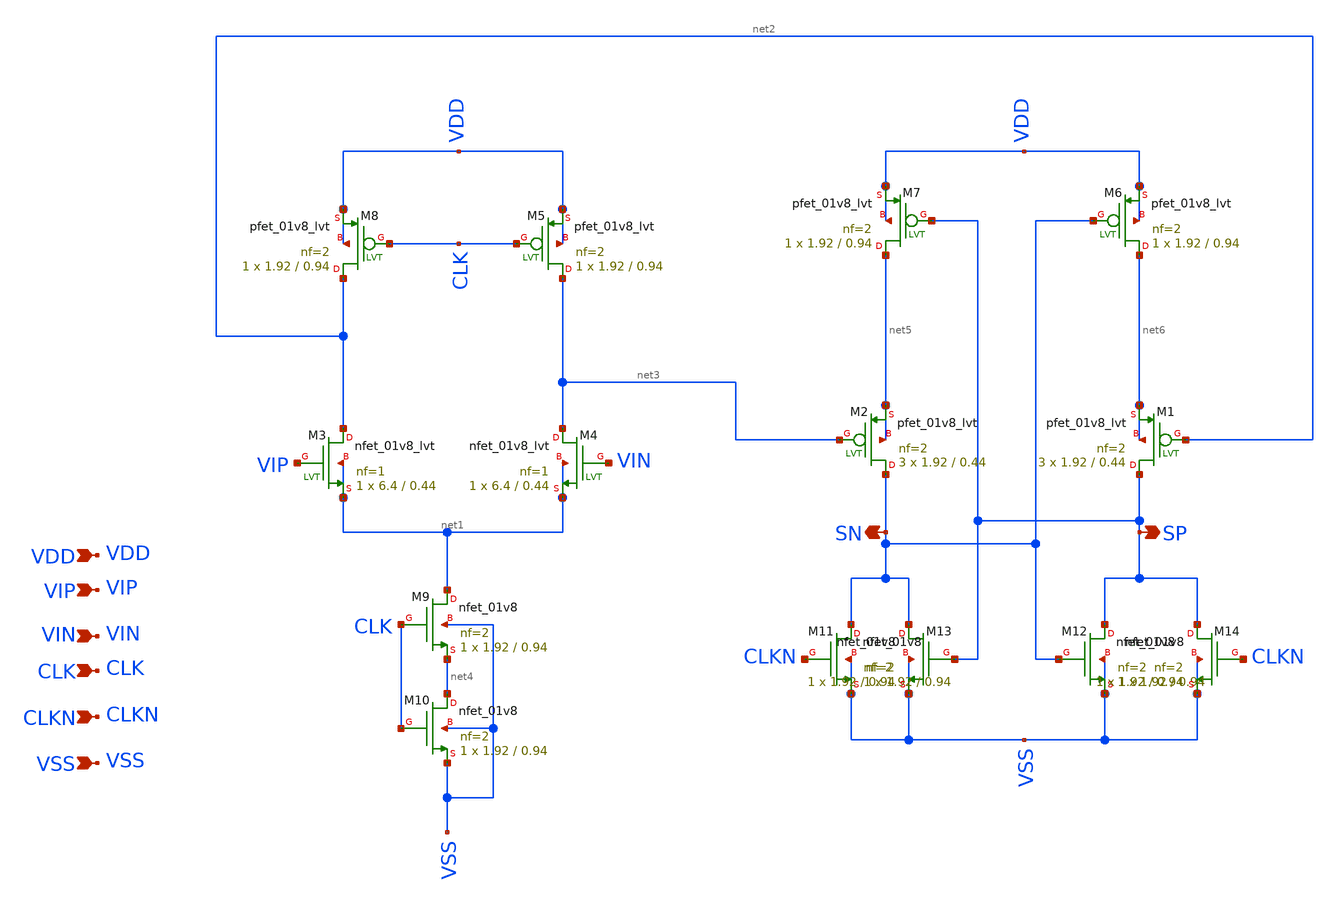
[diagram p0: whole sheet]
** sch_path: design/LELO_SVOD_SKY130A/LELO_CMP.sch
**.subckt LELO_CMP VIP VIN CLK CLKN VDD VSS SN SP
*.ipin VIP
*.ipin VIN
*.ipin CLK
*.ipin CLKN
*.ipin VDD
*.ipin VSS
*.opin SN
*.opin SP
XM2 SN net3 net5 net5 sky130_fd_pr__pfet_01v8_lvt L=0.44 W=1.92 nf=2 ad='int((2 + 1)/2) * 1.92 / 2 * 0.29'
+ as='int((2 + 2)/2) * 1.92 / 2 * 0.29' pd='2*int((2 + 1)/2) * (1.92 / 2 + 0.29)' ps='2*int((2 + 2)/2) * (1.92 / 2 + 0.29)'
+ nrd='0.29 / 1.92 ' nrs='0.29 / 1.92 ' sa=0 sb=0 sd=0 mult=3 m=3
XM1 SP net2 net6 net6 sky130_fd_pr__pfet_01v8_lvt L=0.44 W=1.92 nf=2 ad='int((2 + 1)/2) * 1.92 / 2 * 0.29'
+ as='int((2 + 2)/2) * 1.92 / 2 * 0.29' pd='2*int((2 + 1)/2) * (1.92 / 2 + 0.29)' ps='2*int((2 + 2)/2) * (1.92 / 2 + 0.29)'
+ nrd='0.29 / 1.92 ' nrs='0.29 / 1.92 ' sa=0 sb=0 sd=0 mult=3 m=3
XM3 net2 VIP net1 net1 sky130_fd_pr__nfet_01v8_lvt L=0.44 W=6.4 nf=1 ad='int((1 + 1)/2) * 6.4 / 1 * 0.29'
+ as='int((1 + 2)/2) * 6.4 / 1 * 0.29' pd='2*int((1 + 1)/2) * (6.4 / 1 + 0.29)' ps='2*int((1 + 2)/2) * (6.4 / 1 + 0.29)'
+ nrd='0.29 / 6.4 ' nrs='0.29 / 6.4 ' sa=0 sb=0 sd=0 mult=1 m=1
XM4 net3 VIN net1 net1 sky130_fd_pr__nfet_01v8_lvt L=0.44 W=6.4 nf=1 ad='int((1 + 1)/2) * 6.4 / 1 * 0.29'
+ as='int((1 + 2)/2) * 6.4 / 1 * 0.29' pd='2*int((1 + 1)/2) * (6.4 / 1 + 0.29)' ps='2*int((1 + 2)/2) * (6.4 / 1 + 0.29)'
+ nrd='0.29 / 6.4 ' nrs='0.29 / 6.4 ' sa=0 sb=0 sd=0 mult=1 m=1
XM5 net3 CLK VDD VDD sky130_fd_pr__pfet_01v8_lvt L=0.94 W=1.92 nf=2 ad='int((2 + 1)/2) * 1.92 / 2 * 0.29'
+ as='int((2 + 2)/2) * 1.92 / 2 * 0.29' pd='2*int((2 + 1)/2) * (1.92 / 2 + 0.29)' ps='2*int((2 + 2)/2) * (1.92 / 2 + 0.29)'
+ nrd='0.29 / 1.92 ' nrs='0.29 / 1.92 ' sa=0 sb=0 sd=0 mult=1 m=1
XM6 net6 SN VDD VDD sky130_fd_pr__pfet_01v8_lvt L=0.94 W=1.92 nf=2 ad='int((2 + 1)/2) * 1.92 / 2 * 0.29'
+ as='int((2 + 2)/2) * 1.92 / 2 * 0.29' pd='2*int((2 + 1)/2) * (1.92 / 2 + 0.29)' ps='2*int((2 + 2)/2) * (1.92 / 2 + 0.29)'
+ nrd='0.29 / 1.92 ' nrs='0.29 / 1.92 ' sa=0 sb=0 sd=0 mult=1 m=1
XM7 net5 SP VDD VDD sky130_fd_pr__pfet_01v8_lvt L=0.94 W=1.92 nf=2 ad='int((2 + 1)/2) * 1.92 / 2 * 0.29'
+ as='int((2 + 2)/2) * 1.92 / 2 * 0.29' pd='2*int((2 + 1)/2) * (1.92 / 2 + 0.29)' ps='2*int((2 + 2)/2) * (1.92 / 2 + 0.29)'
+ nrd='0.29 / 1.92 ' nrs='0.29 / 1.92 ' sa=0 sb=0 sd=0 mult=1 m=1
XM8 net2 CLK VDD VDD sky130_fd_pr__pfet_01v8_lvt L=0.94 W=1.92 nf=2 ad='int((2 + 1)/2) * 1.92 / 2 * 0.29'
+ as='int((2 + 2)/2) * 1.92 / 2 * 0.29' pd='2*int((2 + 1)/2) * (1.92 / 2 + 0.29)' ps='2*int((2 + 2)/2) * (1.92 / 2 + 0.29)'
+ nrd='0.29 / 1.92 ' nrs='0.29 / 1.92 ' sa=0 sb=0 sd=0 mult=1 m=1
XM9 net1 CLK net4 VSS sky130_fd_pr__nfet_01v8 L=0.94 W=1.92 nf=2 ad='int((2 + 1)/2) * 1.92 / 2 * 0.29'
+ as='int((2 + 2)/2) * 1.92 / 2 * 0.29' pd='2*int((2 + 1)/2) * (1.92 / 2 + 0.29)' ps='2*int((2 + 2)/2) * (1.92 / 2 + 0.29)'
+ nrd='0.29 / 1.92 ' nrs='0.29 / 1.92 ' sa=0 sb=0 sd=0 mult=1 m=1
XM10 net4 CLK VSS VSS sky130_fd_pr__nfet_01v8 L=0.94 W=1.92 nf=2 ad='int((2 + 1)/2) * 1.92 / 2 * 0.29'
+ as='int((2 + 2)/2) * 1.92 / 2 * 0.29' pd='2*int((2 + 1)/2) * (1.92 / 2 + 0.29)' ps='2*int((2 + 2)/2) * (1.92 / 2 + 0.29)'
+ nrd='0.29 / 1.92 ' nrs='0.29 / 1.92 ' sa=0 sb=0 sd=0 mult=1 m=1
XM11 SN CLKN VSS VSS sky130_fd_pr__nfet_01v8 L=0.94 W=1.92 nf=2 ad='int((2 + 1)/2) * 1.92 / 2 * 0.29'
+ as='int((2 + 2)/2) * 1.92 / 2 * 0.29' pd='2*int((2 + 1)/2) * (1.92 / 2 + 0.29)' ps='2*int((2 + 2)/2) * (1.92 / 2 + 0.29)'
+ nrd='0.29 / 1.92 ' nrs='0.29 / 1.92 ' sa=0 sb=0 sd=0 mult=1 m=1
XM12 SP SN VSS VSS sky130_fd_pr__nfet_01v8 L=0.94 W=1.92 nf=2 ad='int((2 + 1)/2) * 1.92 / 2 * 0.29' as='int((2 + 2)/2) * 1.92 / 2 * 0.29'
+ pd='2*int((2 + 1)/2) * (1.92 / 2 + 0.29)' ps='2*int((2 + 2)/2) * (1.92 / 2 + 0.29)' nrd='0.29 / 1.92 '
+ nrs='0.29 / 1.92 ' sa=0 sb=0 sd=0 mult=1 m=1
XM13 SN SP VSS VSS sky130_fd_pr__nfet_01v8 L=0.94 W=1.92 nf=2 ad='int((2 + 1)/2) * 1.92 / 2 * 0.29' as='int((2 + 2)/2) * 1.92 / 2 * 0.29'
+ pd='2*int((2 + 1)/2) * (1.92 / 2 + 0.29)' ps='2*int((2 + 2)/2) * (1.92 / 2 + 0.29)' nrd='0.29 / 1.92 '
+ nrs='0.29 / 1.92 ' sa=0 sb=0 sd=0 mult=1 m=1
XM14 SP CLKN VSS VSS sky130_fd_pr__nfet_01v8 L=0.94 W=1.92 nf=2 ad='int((2 + 1)/2) * 1.92 / 2 * 0.29'
+ as='int((2 + 2)/2) * 1.92 / 2 * 0.29' pd='2*int((2 + 1)/2) * (1.92 / 2 + 0.29)' ps='2*int((2 + 2)/2) * (1.92 / 2 + 0.29)'
+ nrd='0.29 / 1.92 ' nrs='0.29 / 1.92 ' sa=0 sb=0 sd=0 mult=1 m=1
**.ends
.end
